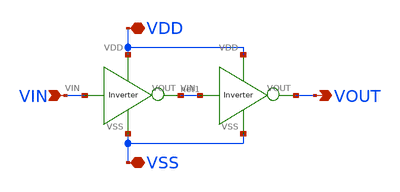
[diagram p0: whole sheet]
** sch_path: xschem/DC_DC_Converter_xschem/OTHERS/DC_DC_Converter0/Buffer.sch
**.subckt Buffer VIN VDD VSS VOUT
*.ipin VIN
*.iopin VDD
*.iopin VSS
*.opin VOUT
X1 VIN net1 VDD VSS Inverter
X2 net1 VOUT VDD VSS Inverter
**.ends
.end
